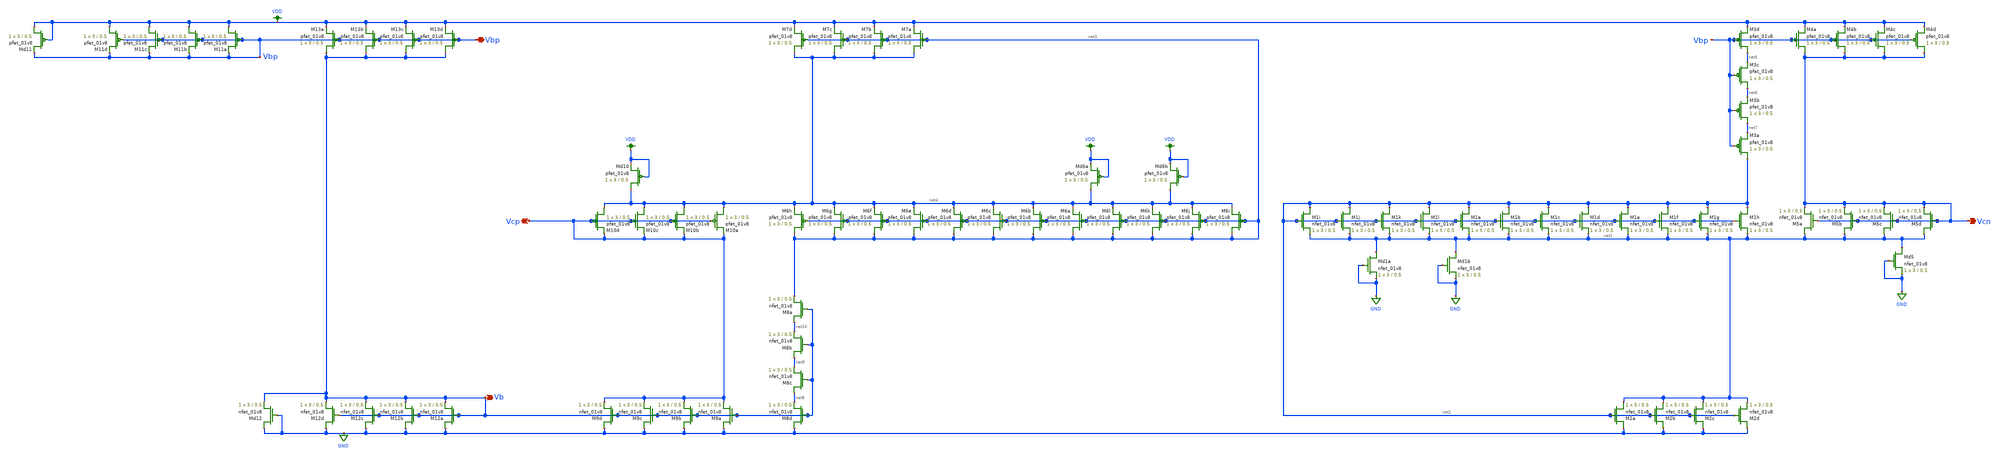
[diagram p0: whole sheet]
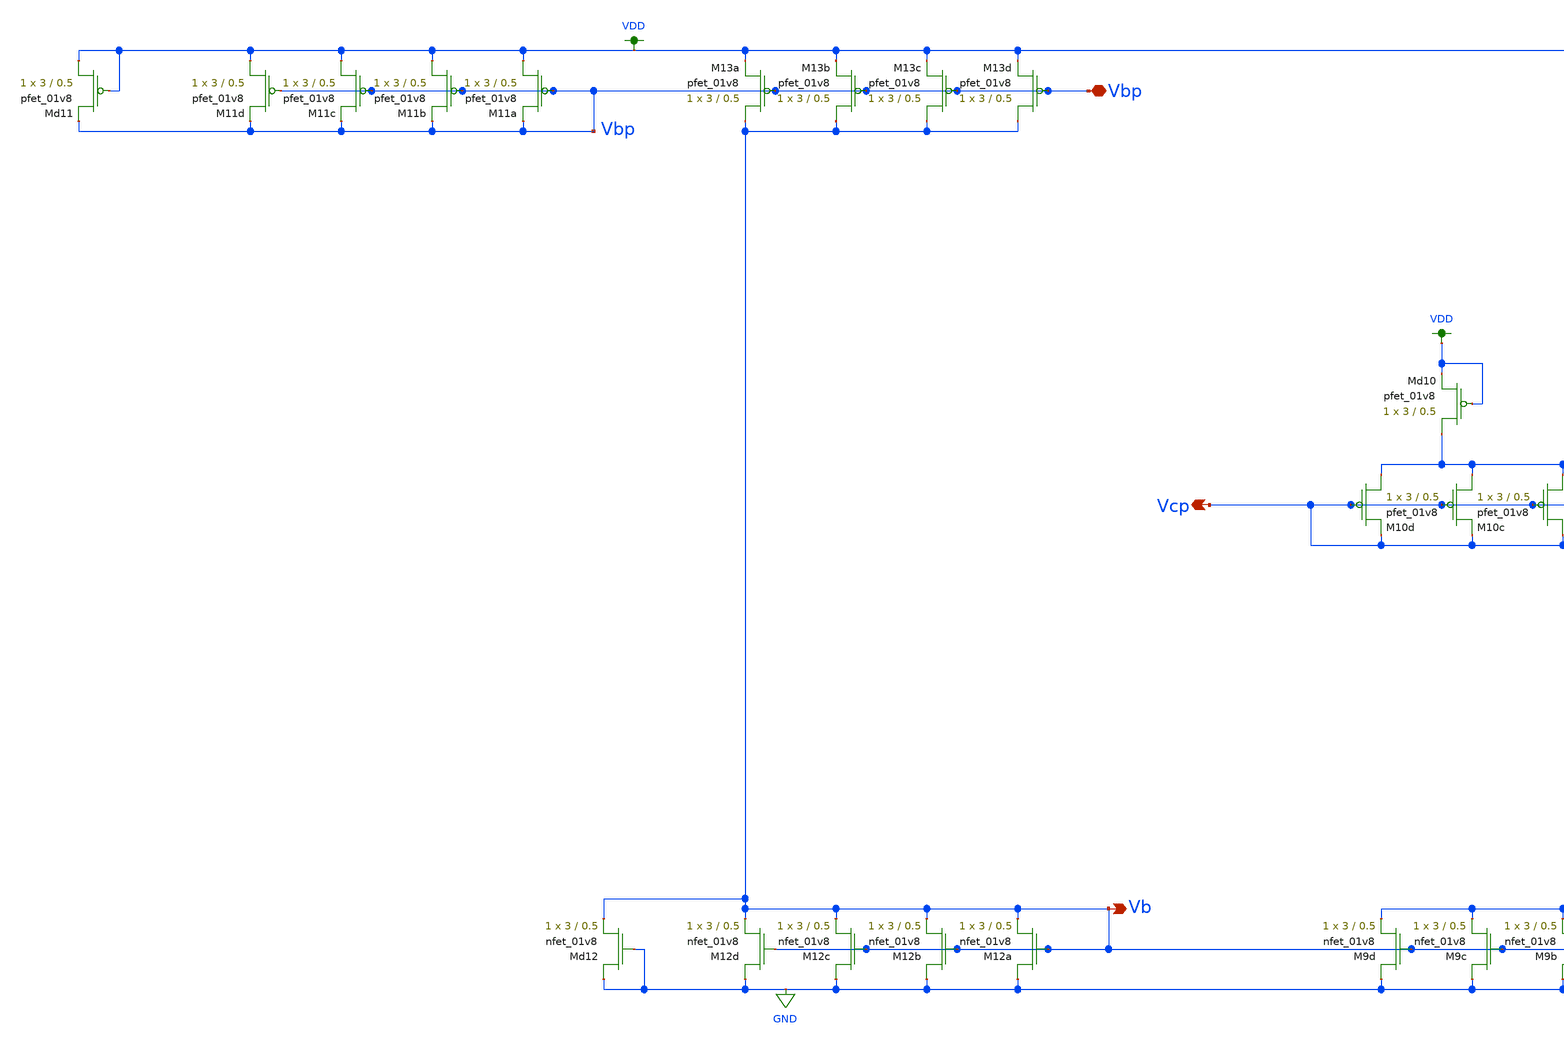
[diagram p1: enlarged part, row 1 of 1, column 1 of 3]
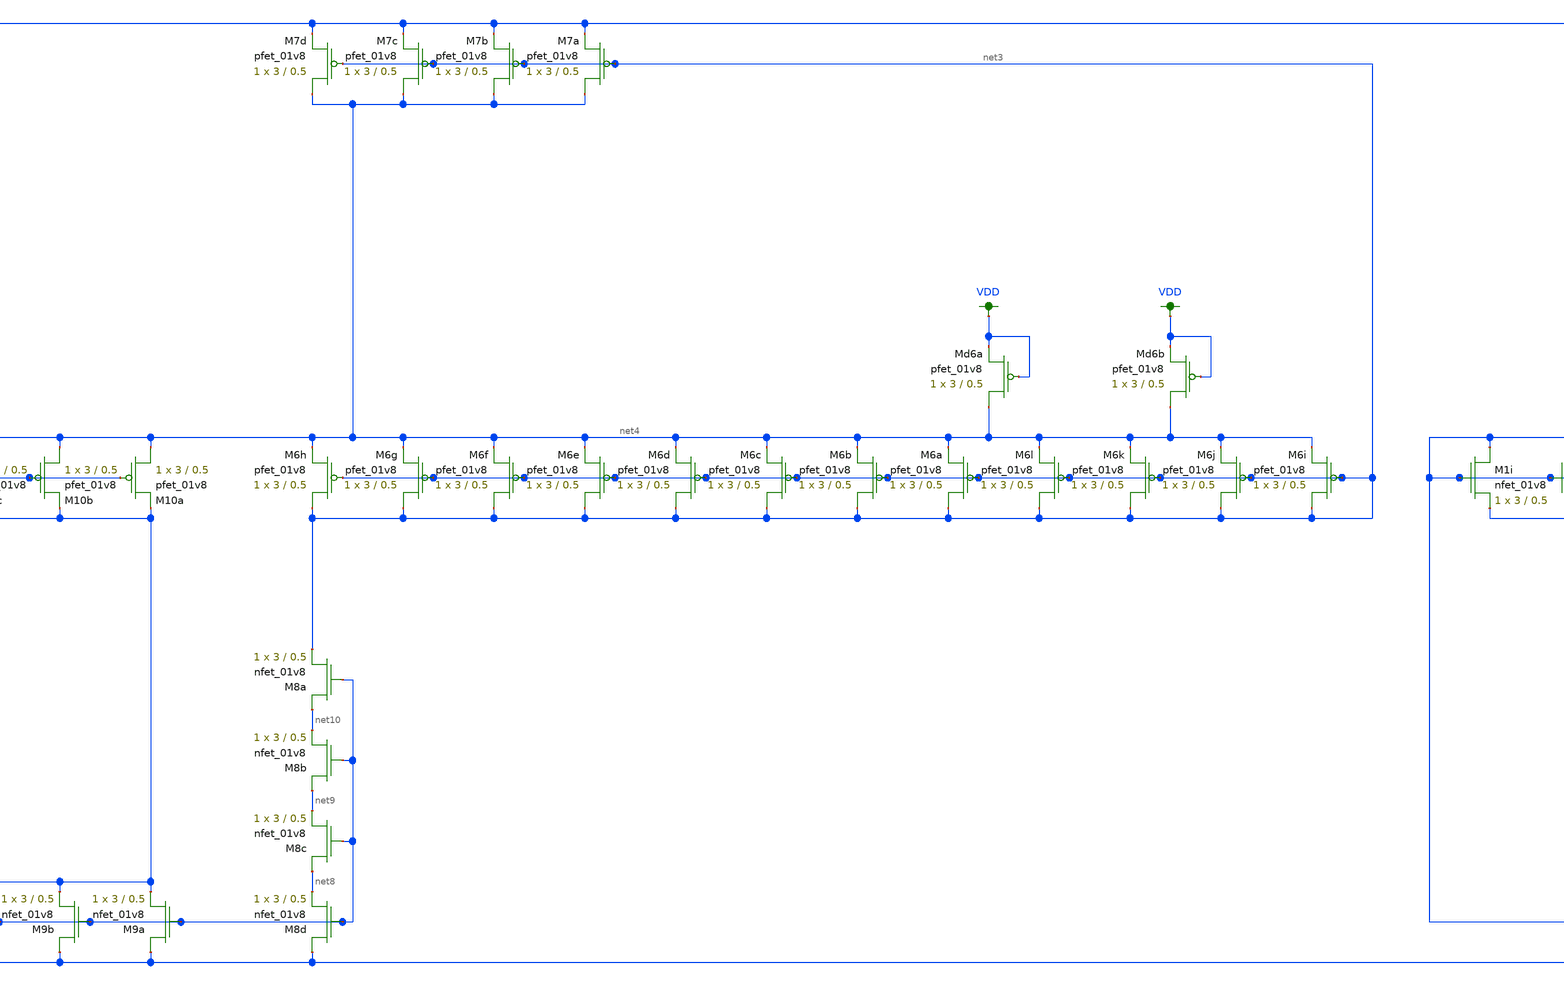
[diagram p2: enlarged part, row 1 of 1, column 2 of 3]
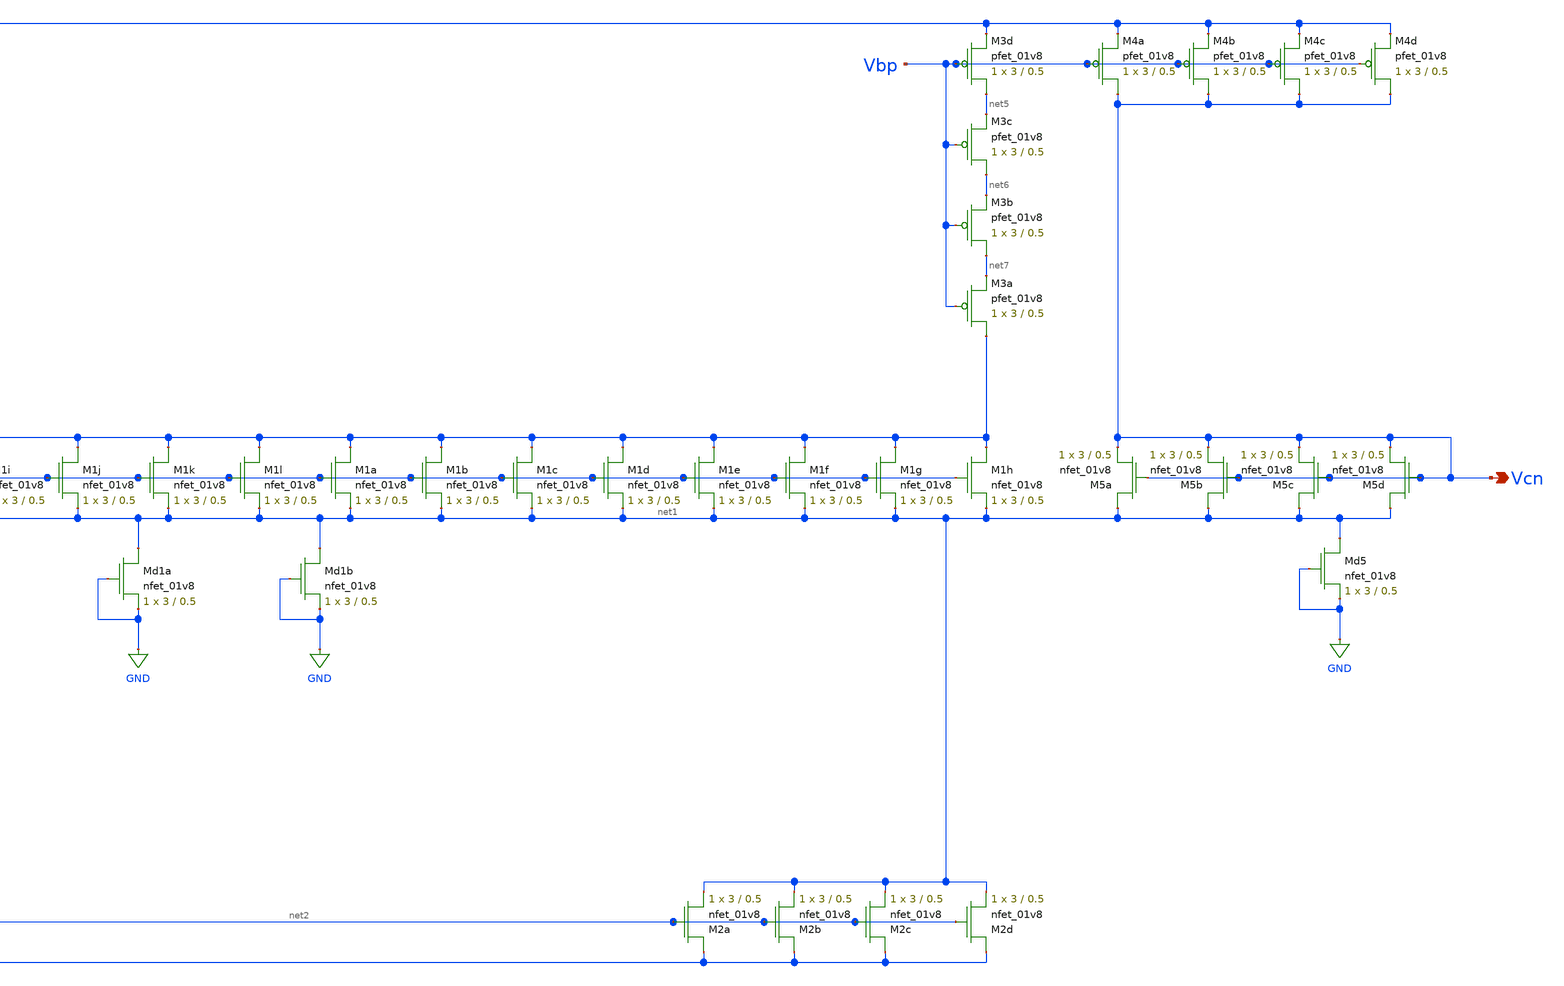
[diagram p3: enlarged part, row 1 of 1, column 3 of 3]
** sch_path: xschem/other_project_files/bias_schematic_lvs.sch
**.subckt bias_schematic_lvs Vcp Vbp Vcn Vb
*.opin Vcp
*.iopin Vbp
*.opin Vcn
*.opin Vb
XM1a net2 net2 net1 GND sky130_fd_pr__nfet_01v8 L=0.5 W=3 nf=1 ad='int((nf+1)/2) * W/nf * 0.29' as='int((nf+2)/2) * W/nf * 0.29'
+ pd='2*int((nf+1)/2) * (W/nf + 0.29)' ps='2*int((nf+2)/2) * (W/nf + 0.29)' nrd='0.29 / W' nrs='0.29 / W'
+ sa=0 sb=0 sd=0 mult=1 m=1
XM1b net2 net2 net1 GND sky130_fd_pr__nfet_01v8 L=0.5 W=3 nf=1 ad='int((nf+1)/2) * W/nf * 0.29' as='int((nf+2)/2) * W/nf * 0.29'
+ pd='2*int((nf+1)/2) * (W/nf + 0.29)' ps='2*int((nf+2)/2) * (W/nf + 0.29)' nrd='0.29 / W' nrs='0.29 / W'
+ sa=0 sb=0 sd=0 mult=1 m=1
XM1c net2 net2 net1 GND sky130_fd_pr__nfet_01v8 L=0.5 W=3 nf=1 ad='int((nf+1)/2) * W/nf * 0.29' as='int((nf+2)/2) * W/nf * 0.29'
+ pd='2*int((nf+1)/2) * (W/nf + 0.29)' ps='2*int((nf+2)/2) * (W/nf + 0.29)' nrd='0.29 / W' nrs='0.29 / W'
+ sa=0 sb=0 sd=0 mult=1 m=1
XM1d net2 net2 net1 GND sky130_fd_pr__nfet_01v8 L=0.5 W=3 nf=1 ad='int((nf+1)/2) * W/nf * 0.29' as='int((nf+2)/2) * W/nf * 0.29'
+ pd='2*int((nf+1)/2) * (W/nf + 0.29)' ps='2*int((nf+2)/2) * (W/nf + 0.29)' nrd='0.29 / W' nrs='0.29 / W'
+ sa=0 sb=0 sd=0 mult=1 m=1
XM2a GND net2 net1 GND sky130_fd_pr__nfet_01v8 L=0.5 W=3 nf=1 ad='int((nf+1)/2) * W/nf * 0.29' as='int((nf+2)/2) * W/nf * 0.29'
+ pd='2*int((nf+1)/2) * (W/nf + 0.29)' ps='2*int((nf+2)/2) * (W/nf + 0.29)' nrd='0.29 / W' nrs='0.29 / W'
+ sa=0 sb=0 sd=0 mult=1 m=1
XM2b GND net2 net1 GND sky130_fd_pr__nfet_01v8 L=0.5 W=3 nf=1 ad='int((nf+1)/2) * W/nf * 0.29' as='int((nf+2)/2) * W/nf * 0.29'
+ pd='2*int((nf+1)/2) * (W/nf + 0.29)' ps='2*int((nf+2)/2) * (W/nf + 0.29)' nrd='0.29 / W' nrs='0.29 / W'
+ sa=0 sb=0 sd=0 mult=1 m=1
XM2c GND net2 net1 GND sky130_fd_pr__nfet_01v8 L=0.5 W=3 nf=1 ad='int((nf+1)/2) * W/nf * 0.29' as='int((nf+2)/2) * W/nf * 0.29'
+ pd='2*int((nf+1)/2) * (W/nf + 0.29)' ps='2*int((nf+2)/2) * (W/nf + 0.29)' nrd='0.29 / W' nrs='0.29 / W'
+ sa=0 sb=0 sd=0 mult=1 m=1
XM2d GND net2 net1 GND sky130_fd_pr__nfet_01v8 L=0.5 W=3 nf=1 ad='int((nf+1)/2) * W/nf * 0.29' as='int((nf+2)/2) * W/nf * 0.29'
+ pd='2*int((nf+1)/2) * (W/nf + 0.29)' ps='2*int((nf+2)/2) * (W/nf + 0.29)' nrd='0.29 / W' nrs='0.29 / W'
+ sa=0 sb=0 sd=0 mult=1 m=1
XM3a net2 Vbp net7 VDD sky130_fd_pr__pfet_01v8 L=0.5 W=3 nf=1 ad='int((nf+1)/2) * W/nf * 0.29' as='int((nf+2)/2) * W/nf * 0.29'
+ pd='2*int((nf+1)/2) * (W/nf + 0.29)' ps='2*int((nf+2)/2) * (W/nf + 0.29)' nrd='0.29 / W' nrs='0.29 / W'
+ sa=0 sb=0 sd=0 mult=1 m=1
XM3b net7 Vbp net6 VDD sky130_fd_pr__pfet_01v8 L=0.5 W=3 nf=1 ad='int((nf+1)/2) * W/nf * 0.29' as='int((nf+2)/2) * W/nf * 0.29'
+ pd='2*int((nf+1)/2) * (W/nf + 0.29)' ps='2*int((nf+2)/2) * (W/nf + 0.29)' nrd='0.29 / W' nrs='0.29 / W'
+ sa=0 sb=0 sd=0 mult=1 m=1
XM3c net6 Vbp net5 VDD sky130_fd_pr__pfet_01v8 L=0.5 W=3 nf=1 ad='int((nf+1)/2) * W/nf * 0.29' as='int((nf+2)/2) * W/nf * 0.29'
+ pd='2*int((nf+1)/2) * (W/nf + 0.29)' ps='2*int((nf+2)/2) * (W/nf + 0.29)' nrd='0.29 / W' nrs='0.29 / W'
+ sa=0 sb=0 sd=0 mult=1 m=1
XM3d net5 Vbp VDD VDD sky130_fd_pr__pfet_01v8 L=0.5 W=3 nf=1 ad='int((nf+1)/2) * W/nf * 0.29' as='int((nf+2)/2) * W/nf * 0.29'
+ pd='2*int((nf+1)/2) * (W/nf + 0.29)' ps='2*int((nf+2)/2) * (W/nf + 0.29)' nrd='0.29 / W' nrs='0.29 / W'
+ sa=0 sb=0 sd=0 mult=1 m=1
XM4a Vcn Vbp VDD VDD sky130_fd_pr__pfet_01v8 L=0.5 W=3 nf=1 ad='int((nf+1)/2) * W/nf * 0.29' as='int((nf+2)/2) * W/nf * 0.29'
+ pd='2*int((nf+1)/2) * (W/nf + 0.29)' ps='2*int((nf+2)/2) * (W/nf + 0.29)' nrd='0.29 / W' nrs='0.29 / W'
+ sa=0 sb=0 sd=0 mult=1 m=1
XM4b Vcn Vbp VDD VDD sky130_fd_pr__pfet_01v8 L=0.5 W=3 nf=1 ad='int((nf+1)/2) * W/nf * 0.29' as='int((nf+2)/2) * W/nf * 0.29'
+ pd='2*int((nf+1)/2) * (W/nf + 0.29)' ps='2*int((nf+2)/2) * (W/nf + 0.29)' nrd='0.29 / W' nrs='0.29 / W'
+ sa=0 sb=0 sd=0 mult=1 m=1
XM4c Vcn Vbp VDD VDD sky130_fd_pr__pfet_01v8 L=0.5 W=3 nf=1 ad='int((nf+1)/2) * W/nf * 0.29' as='int((nf+2)/2) * W/nf * 0.29'
+ pd='2*int((nf+1)/2) * (W/nf + 0.29)' ps='2*int((nf+2)/2) * (W/nf + 0.29)' nrd='0.29 / W' nrs='0.29 / W'
+ sa=0 sb=0 sd=0 mult=1 m=1
XM4d Vcn Vbp VDD VDD sky130_fd_pr__pfet_01v8 L=0.5 W=3 nf=1 ad='int((nf+1)/2) * W/nf * 0.29' as='int((nf+2)/2) * W/nf * 0.29'
+ pd='2*int((nf+1)/2) * (W/nf + 0.29)' ps='2*int((nf+2)/2) * (W/nf + 0.29)' nrd='0.29 / W' nrs='0.29 / W'
+ sa=0 sb=0 sd=0 mult=1 m=1
XM11a VDD Vbp Vbp VDD sky130_fd_pr__pfet_01v8 L=0.5 W=3 nf=1 ad='int((nf+1)/2) * W/nf * 0.29' as='int((nf+2)/2) * W/nf * 0.29'
+ pd='2*int((nf+1)/2) * (W/nf + 0.29)' ps='2*int((nf+2)/2) * (W/nf + 0.29)' nrd='0.29 / W' nrs='0.29 / W'
+ sa=0 sb=0 sd=0 mult=1 m=1
XM11b VDD Vbp Vbp VDD sky130_fd_pr__pfet_01v8 L=0.5 W=3 nf=1 ad='int((nf+1)/2) * W/nf * 0.29' as='int((nf+2)/2) * W/nf * 0.29'
+ pd='2*int((nf+1)/2) * (W/nf + 0.29)' ps='2*int((nf+2)/2) * (W/nf + 0.29)' nrd='0.29 / W' nrs='0.29 / W'
+ sa=0 sb=0 sd=0 mult=1 m=1
XM11c VDD Vbp Vbp VDD sky130_fd_pr__pfet_01v8 L=0.5 W=3 nf=1 ad='int((nf+1)/2) * W/nf * 0.29' as='int((nf+2)/2) * W/nf * 0.29'
+ pd='2*int((nf+1)/2) * (W/nf + 0.29)' ps='2*int((nf+2)/2) * (W/nf + 0.29)' nrd='0.29 / W' nrs='0.29 / W'
+ sa=0 sb=0 sd=0 mult=1 m=1
XM11d VDD Vbp Vbp VDD sky130_fd_pr__pfet_01v8 L=0.5 W=3 nf=1 ad='int((nf+1)/2) * W/nf * 0.29' as='int((nf+2)/2) * W/nf * 0.29'
+ pd='2*int((nf+1)/2) * (W/nf + 0.29)' ps='2*int((nf+2)/2) * (W/nf + 0.29)' nrd='0.29 / W' nrs='0.29 / W'
+ sa=0 sb=0 sd=0 mult=1 m=1
XM5a net1 Vcn Vcn GND sky130_fd_pr__nfet_01v8 L=0.5 W=3 nf=1 ad='int((nf+1)/2) * W/nf * 0.29' as='int((nf+2)/2) * W/nf * 0.29'
+ pd='2*int((nf+1)/2) * (W/nf + 0.29)' ps='2*int((nf+2)/2) * (W/nf + 0.29)' nrd='0.29 / W' nrs='0.29 / W'
+ sa=0 sb=0 sd=0 mult=1 m=1
XM5b net1 Vcn Vcn GND sky130_fd_pr__nfet_01v8 L=0.5 W=3 nf=1 ad='int((nf+1)/2) * W/nf * 0.29' as='int((nf+2)/2) * W/nf * 0.29'
+ pd='2*int((nf+1)/2) * (W/nf + 0.29)' ps='2*int((nf+2)/2) * (W/nf + 0.29)' nrd='0.29 / W' nrs='0.29 / W'
+ sa=0 sb=0 sd=0 mult=1 m=1
XM5c net1 Vcn Vcn GND sky130_fd_pr__nfet_01v8 L=0.5 W=3 nf=1 ad='int((nf+1)/2) * W/nf * 0.29' as='int((nf+2)/2) * W/nf * 0.29'
+ pd='2*int((nf+1)/2) * (W/nf + 0.29)' ps='2*int((nf+2)/2) * (W/nf + 0.29)' nrd='0.29 / W' nrs='0.29 / W'
+ sa=0 sb=0 sd=0 mult=1 m=1
XM5d net1 Vcn Vcn GND sky130_fd_pr__nfet_01v8 L=0.5 W=3 nf=1 ad='int((nf+1)/2) * W/nf * 0.29' as='int((nf+2)/2) * W/nf * 0.29'
+ pd='2*int((nf+1)/2) * (W/nf + 0.29)' ps='2*int((nf+2)/2) * (W/nf + 0.29)' nrd='0.29 / W' nrs='0.29 / W'
+ sa=0 sb=0 sd=0 mult=1 m=1
XM8a net10 Vb net3 GND sky130_fd_pr__nfet_01v8 L=0.5 W=3 nf=1 ad='int((nf+1)/2) * W/nf * 0.29' as='int((nf+2)/2) * W/nf * 0.29'
+ pd='2*int((nf+1)/2) * (W/nf + 0.29)' ps='2*int((nf+2)/2) * (W/nf + 0.29)' nrd='0.29 / W' nrs='0.29 / W'
+ sa=0 sb=0 sd=0 mult=1 m=1
XM8b net9 Vb net10 GND sky130_fd_pr__nfet_01v8 L=0.5 W=3 nf=1 ad='int((nf+1)/2) * W/nf * 0.29' as='int((nf+2)/2) * W/nf * 0.29'
+ pd='2*int((nf+1)/2) * (W/nf + 0.29)' ps='2*int((nf+2)/2) * (W/nf + 0.29)' nrd='0.29 / W' nrs='0.29 / W'
+ sa=0 sb=0 sd=0 mult=1 m=1
XM8c net8 Vb net9 GND sky130_fd_pr__nfet_01v8 L=0.5 W=3 nf=1 ad='int((nf+1)/2) * W/nf * 0.29' as='int((nf+2)/2) * W/nf * 0.29'
+ pd='2*int((nf+1)/2) * (W/nf + 0.29)' ps='2*int((nf+2)/2) * (W/nf + 0.29)' nrd='0.29 / W' nrs='0.29 / W'
+ sa=0 sb=0 sd=0 mult=1 m=1
XM8d GND Vb net8 GND sky130_fd_pr__nfet_01v8 L=0.5 W=3 nf=1 ad='int((nf+1)/2) * W/nf * 0.29' as='int((nf+2)/2) * W/nf * 0.29'
+ pd='2*int((nf+1)/2) * (W/nf + 0.29)' ps='2*int((nf+2)/2) * (W/nf + 0.29)' nrd='0.29 / W' nrs='0.29 / W'
+ sa=0 sb=0 sd=0 mult=1 m=1
XM6a net3 net3 net4 VDD sky130_fd_pr__pfet_01v8 L=0.5 W=3 nf=1 ad='int((nf+1)/2) * W/nf * 0.29' as='int((nf+2)/2) * W/nf * 0.29'
+ pd='2*int((nf+1)/2) * (W/nf + 0.29)' ps='2*int((nf+2)/2) * (W/nf + 0.29)' nrd='0.29 / W' nrs='0.29 / W'
+ sa=0 sb=0 sd=0 mult=1 m=1
XM6b net3 net3 net4 VDD sky130_fd_pr__pfet_01v8 L=0.5 W=3 nf=1 ad='int((nf+1)/2) * W/nf * 0.29' as='int((nf+2)/2) * W/nf * 0.29'
+ pd='2*int((nf+1)/2) * (W/nf + 0.29)' ps='2*int((nf+2)/2) * (W/nf + 0.29)' nrd='0.29 / W' nrs='0.29 / W'
+ sa=0 sb=0 sd=0 mult=1 m=1
XM6c net3 net3 net4 VDD sky130_fd_pr__pfet_01v8 L=0.5 W=3 nf=1 ad='int((nf+1)/2) * W/nf * 0.29' as='int((nf+2)/2) * W/nf * 0.29'
+ pd='2*int((nf+1)/2) * (W/nf + 0.29)' ps='2*int((nf+2)/2) * (W/nf + 0.29)' nrd='0.29 / W' nrs='0.29 / W'
+ sa=0 sb=0 sd=0 mult=1 m=1
XM6d net3 net3 net4 VDD sky130_fd_pr__pfet_01v8 L=0.5 W=3 nf=1 ad='int((nf+1)/2) * W/nf * 0.29' as='int((nf+2)/2) * W/nf * 0.29'
+ pd='2*int((nf+1)/2) * (W/nf + 0.29)' ps='2*int((nf+2)/2) * (W/nf + 0.29)' nrd='0.29 / W' nrs='0.29 / W'
+ sa=0 sb=0 sd=0 mult=1 m=1
XM7a net4 net3 VDD VDD sky130_fd_pr__pfet_01v8 L=0.5 W=3 nf=1 ad='int((nf+1)/2) * W/nf * 0.29' as='int((nf+2)/2) * W/nf * 0.29'
+ pd='2*int((nf+1)/2) * (W/nf + 0.29)' ps='2*int((nf+2)/2) * (W/nf + 0.29)' nrd='0.29 / W' nrs='0.29 / W'
+ sa=0 sb=0 sd=0 mult=1 m=1
XM7b net4 net3 VDD VDD sky130_fd_pr__pfet_01v8 L=0.5 W=3 nf=1 ad='int((nf+1)/2) * W/nf * 0.29' as='int((nf+2)/2) * W/nf * 0.29'
+ pd='2*int((nf+1)/2) * (W/nf + 0.29)' ps='2*int((nf+2)/2) * (W/nf + 0.29)' nrd='0.29 / W' nrs='0.29 / W'
+ sa=0 sb=0 sd=0 mult=1 m=1
XM7c net4 net3 VDD VDD sky130_fd_pr__pfet_01v8 L=0.5 W=3 nf=1 ad='int((nf+1)/2) * W/nf * 0.29' as='int((nf+2)/2) * W/nf * 0.29'
+ pd='2*int((nf+1)/2) * (W/nf + 0.29)' ps='2*int((nf+2)/2) * (W/nf + 0.29)' nrd='0.29 / W' nrs='0.29 / W'
+ sa=0 sb=0 sd=0 mult=1 m=1
XM7d net4 net3 VDD VDD sky130_fd_pr__pfet_01v8 L=0.5 W=3 nf=1 ad='int((nf+1)/2) * W/nf * 0.29' as='int((nf+2)/2) * W/nf * 0.29'
+ pd='2*int((nf+1)/2) * (W/nf + 0.29)' ps='2*int((nf+2)/2) * (W/nf + 0.29)' nrd='0.29 / W' nrs='0.29 / W'
+ sa=0 sb=0 sd=0 mult=1 m=1
XM10d net4 Vcp Vcp VDD sky130_fd_pr__pfet_01v8 L=0.5 W=3 nf=1 ad='int((nf+1)/2) * W/nf * 0.29' as='int((nf+2)/2) * W/nf * 0.29'
+ pd='2*int((nf+1)/2) * (W/nf + 0.29)' ps='2*int((nf+2)/2) * (W/nf + 0.29)' nrd='0.29 / W' nrs='0.29 / W'
+ sa=0 sb=0 sd=0 mult=1 m=1
XM10c net4 Vcp Vcp VDD sky130_fd_pr__pfet_01v8 L=0.5 W=3 nf=1 ad='int((nf+1)/2) * W/nf * 0.29' as='int((nf+2)/2) * W/nf * 0.29'
+ pd='2*int((nf+1)/2) * (W/nf + 0.29)' ps='2*int((nf+2)/2) * (W/nf + 0.29)' nrd='0.29 / W' nrs='0.29 / W'
+ sa=0 sb=0 sd=0 mult=1 m=1
XM10b net4 Vcp Vcp VDD sky130_fd_pr__pfet_01v8 L=0.5 W=3 nf=1 ad='int((nf+1)/2) * W/nf * 0.29' as='int((nf+2)/2) * W/nf * 0.29'
+ pd='2*int((nf+1)/2) * (W/nf + 0.29)' ps='2*int((nf+2)/2) * (W/nf + 0.29)' nrd='0.29 / W' nrs='0.29 / W'
+ sa=0 sb=0 sd=0 mult=1 m=1
XM10a net4 Vcp Vcp VDD sky130_fd_pr__pfet_01v8 L=0.5 W=3 nf=1 ad='int((nf+1)/2) * W/nf * 0.29' as='int((nf+2)/2) * W/nf * 0.29'
+ pd='2*int((nf+1)/2) * (W/nf + 0.29)' ps='2*int((nf+2)/2) * (W/nf + 0.29)' nrd='0.29 / W' nrs='0.29 / W'
+ sa=0 sb=0 sd=0 mult=1 m=1
XM9a GND Vb Vcp GND sky130_fd_pr__nfet_01v8 L=0.5 W=3 nf=1 ad='int((nf+1)/2) * W/nf * 0.29' as='int((nf+2)/2) * W/nf * 0.29'
+ pd='2*int((nf+1)/2) * (W/nf + 0.29)' ps='2*int((nf+2)/2) * (W/nf + 0.29)' nrd='0.29 / W' nrs='0.29 / W'
+ sa=0 sb=0 sd=0 mult=1 m=1
XM9b GND Vb Vcp GND sky130_fd_pr__nfet_01v8 L=0.5 W=3 nf=1 ad='int((nf+1)/2) * W/nf * 0.29' as='int((nf+2)/2) * W/nf * 0.29'
+ pd='2*int((nf+1)/2) * (W/nf + 0.29)' ps='2*int((nf+2)/2) * (W/nf + 0.29)' nrd='0.29 / W' nrs='0.29 / W'
+ sa=0 sb=0 sd=0 mult=1 m=1
XM9c GND Vb Vcp GND sky130_fd_pr__nfet_01v8 L=0.5 W=3 nf=1 ad='int((nf+1)/2) * W/nf * 0.29' as='int((nf+2)/2) * W/nf * 0.29'
+ pd='2*int((nf+1)/2) * (W/nf + 0.29)' ps='2*int((nf+2)/2) * (W/nf + 0.29)' nrd='0.29 / W' nrs='0.29 / W'
+ sa=0 sb=0 sd=0 mult=1 m=1
XM9d GND Vb Vcp GND sky130_fd_pr__nfet_01v8 L=0.5 W=3 nf=1 ad='int((nf+1)/2) * W/nf * 0.29' as='int((nf+2)/2) * W/nf * 0.29'
+ pd='2*int((nf+1)/2) * (W/nf + 0.29)' ps='2*int((nf+2)/2) * (W/nf + 0.29)' nrd='0.29 / W' nrs='0.29 / W'
+ sa=0 sb=0 sd=0 mult=1 m=1
XM12a GND Vb Vb GND sky130_fd_pr__nfet_01v8 L=0.5 W=3 nf=1 ad='int((nf+1)/2) * W/nf * 0.29' as='int((nf+2)/2) * W/nf * 0.29'
+ pd='2*int((nf+1)/2) * (W/nf + 0.29)' ps='2*int((nf+2)/2) * (W/nf + 0.29)' nrd='0.29 / W' nrs='0.29 / W'
+ sa=0 sb=0 sd=0 mult=1 m=1
XM12b GND Vb Vb GND sky130_fd_pr__nfet_01v8 L=0.5 W=3 nf=1 ad='int((nf+1)/2) * W/nf * 0.29' as='int((nf+2)/2) * W/nf * 0.29'
+ pd='2*int((nf+1)/2) * (W/nf + 0.29)' ps='2*int((nf+2)/2) * (W/nf + 0.29)' nrd='0.29 / W' nrs='0.29 / W'
+ sa=0 sb=0 sd=0 mult=1 m=1
XM12c GND Vb Vb GND sky130_fd_pr__nfet_01v8 L=0.5 W=3 nf=1 ad='int((nf+1)/2) * W/nf * 0.29' as='int((nf+2)/2) * W/nf * 0.29'
+ pd='2*int((nf+1)/2) * (W/nf + 0.29)' ps='2*int((nf+2)/2) * (W/nf + 0.29)' nrd='0.29 / W' nrs='0.29 / W'
+ sa=0 sb=0 sd=0 mult=1 m=1
XM12d GND Vb Vb GND sky130_fd_pr__nfet_01v8 L=0.5 W=3 nf=1 ad='int((nf+1)/2) * W/nf * 0.29' as='int((nf+2)/2) * W/nf * 0.29'
+ pd='2*int((nf+1)/2) * (W/nf + 0.29)' ps='2*int((nf+2)/2) * (W/nf + 0.29)' nrd='0.29 / W' nrs='0.29 / W'
+ sa=0 sb=0 sd=0 mult=1 m=1
XM13d Vb Vbp VDD VDD sky130_fd_pr__pfet_01v8 L=0.5 W=3 nf=1 ad='int((nf+1)/2) * W/nf * 0.29' as='int((nf+2)/2) * W/nf * 0.29'
+ pd='2*int((nf+1)/2) * (W/nf + 0.29)' ps='2*int((nf+2)/2) * (W/nf + 0.29)' nrd='0.29 / W' nrs='0.29 / W'
+ sa=0 sb=0 sd=0 mult=1 m=1
XM13c Vb Vbp VDD VDD sky130_fd_pr__pfet_01v8 L=0.5 W=3 nf=1 ad='int((nf+1)/2) * W/nf * 0.29' as='int((nf+2)/2) * W/nf * 0.29'
+ pd='2*int((nf+1)/2) * (W/nf + 0.29)' ps='2*int((nf+2)/2) * (W/nf + 0.29)' nrd='0.29 / W' nrs='0.29 / W'
+ sa=0 sb=0 sd=0 mult=1 m=1
XM13b Vb Vbp VDD VDD sky130_fd_pr__pfet_01v8 L=0.5 W=3 nf=1 ad='int((nf+1)/2) * W/nf * 0.29' as='int((nf+2)/2) * W/nf * 0.29'
+ pd='2*int((nf+1)/2) * (W/nf + 0.29)' ps='2*int((nf+2)/2) * (W/nf + 0.29)' nrd='0.29 / W' nrs='0.29 / W'
+ sa=0 sb=0 sd=0 mult=1 m=1
XM13a Vb Vbp VDD VDD sky130_fd_pr__pfet_01v8 L=0.5 W=3 nf=1 ad='int((nf+1)/2) * W/nf * 0.29' as='int((nf+2)/2) * W/nf * 0.29'
+ pd='2*int((nf+1)/2) * (W/nf + 0.29)' ps='2*int((nf+2)/2) * (W/nf + 0.29)' nrd='0.29 / W' nrs='0.29 / W'
+ sa=0 sb=0 sd=0 mult=1 m=1
XM1e net2 net2 net1 GND sky130_fd_pr__nfet_01v8 L=0.5 W=3 nf=1 ad='int((nf+1)/2) * W/nf * 0.29' as='int((nf+2)/2) * W/nf * 0.29'
+ pd='2*int((nf+1)/2) * (W/nf + 0.29)' ps='2*int((nf+2)/2) * (W/nf + 0.29)' nrd='0.29 / W' nrs='0.29 / W'
+ sa=0 sb=0 sd=0 mult=1 m=1
XM1f net2 net2 net1 GND sky130_fd_pr__nfet_01v8 L=0.5 W=3 nf=1 ad='int((nf+1)/2) * W/nf * 0.29' as='int((nf+2)/2) * W/nf * 0.29'
+ pd='2*int((nf+1)/2) * (W/nf + 0.29)' ps='2*int((nf+2)/2) * (W/nf + 0.29)' nrd='0.29 / W' nrs='0.29 / W'
+ sa=0 sb=0 sd=0 mult=1 m=1
XM1g net2 net2 net1 GND sky130_fd_pr__nfet_01v8 L=0.5 W=3 nf=1 ad='int((nf+1)/2) * W/nf * 0.29' as='int((nf+2)/2) * W/nf * 0.29'
+ pd='2*int((nf+1)/2) * (W/nf + 0.29)' ps='2*int((nf+2)/2) * (W/nf + 0.29)' nrd='0.29 / W' nrs='0.29 / W'
+ sa=0 sb=0 sd=0 mult=1 m=1
XM1h net2 net2 net1 GND sky130_fd_pr__nfet_01v8 L=0.5 W=3 nf=1 ad='int((nf+1)/2) * W/nf * 0.29' as='int((nf+2)/2) * W/nf * 0.29'
+ pd='2*int((nf+1)/2) * (W/nf + 0.29)' ps='2*int((nf+2)/2) * (W/nf + 0.29)' nrd='0.29 / W' nrs='0.29 / W'
+ sa=0 sb=0 sd=0 mult=1 m=1
XM6e net3 net3 net4 VDD sky130_fd_pr__pfet_01v8 L=0.5 W=3 nf=1 ad='int((nf+1)/2) * W/nf * 0.29' as='int((nf+2)/2) * W/nf * 0.29'
+ pd='2*int((nf+1)/2) * (W/nf + 0.29)' ps='2*int((nf+2)/2) * (W/nf + 0.29)' nrd='0.29 / W' nrs='0.29 / W'
+ sa=0 sb=0 sd=0 mult=1 m=1
XM6f net3 net3 net4 VDD sky130_fd_pr__pfet_01v8 L=0.5 W=3 nf=1 ad='int((nf+1)/2) * W/nf * 0.29' as='int((nf+2)/2) * W/nf * 0.29'
+ pd='2*int((nf+1)/2) * (W/nf + 0.29)' ps='2*int((nf+2)/2) * (W/nf + 0.29)' nrd='0.29 / W' nrs='0.29 / W'
+ sa=0 sb=0 sd=0 mult=1 m=1
XM6g net3 net3 net4 VDD sky130_fd_pr__pfet_01v8 L=0.5 W=3 nf=1 ad='int((nf+1)/2) * W/nf * 0.29' as='int((nf+2)/2) * W/nf * 0.29'
+ pd='2*int((nf+1)/2) * (W/nf + 0.29)' ps='2*int((nf+2)/2) * (W/nf + 0.29)' nrd='0.29 / W' nrs='0.29 / W'
+ sa=0 sb=0 sd=0 mult=1 m=1
XM6h net3 net3 net4 VDD sky130_fd_pr__pfet_01v8 L=0.5 W=3 nf=1 ad='int((nf+1)/2) * W/nf * 0.29' as='int((nf+2)/2) * W/nf * 0.29'
+ pd='2*int((nf+1)/2) * (W/nf + 0.29)' ps='2*int((nf+2)/2) * (W/nf + 0.29)' nrd='0.29 / W' nrs='0.29 / W'
+ sa=0 sb=0 sd=0 mult=1 m=1
XM1i net2 net2 net1 GND sky130_fd_pr__nfet_01v8 L=0.5 W=3 nf=1 ad='int((nf+1)/2) * W/nf * 0.29' as='int((nf+2)/2) * W/nf * 0.29'
+ pd='2*int((nf+1)/2) * (W/nf + 0.29)' ps='2*int((nf+2)/2) * (W/nf + 0.29)' nrd='0.29 / W' nrs='0.29 / W'
+ sa=0 sb=0 sd=0 mult=1 m=1
XM1j net2 net2 net1 GND sky130_fd_pr__nfet_01v8 L=0.5 W=3 nf=1 ad='int((nf+1)/2) * W/nf * 0.29' as='int((nf+2)/2) * W/nf * 0.29'
+ pd='2*int((nf+1)/2) * (W/nf + 0.29)' ps='2*int((nf+2)/2) * (W/nf + 0.29)' nrd='0.29 / W' nrs='0.29 / W'
+ sa=0 sb=0 sd=0 mult=1 m=1
XM1k net2 net2 net1 GND sky130_fd_pr__nfet_01v8 L=0.5 W=3 nf=1 ad='int((nf+1)/2) * W/nf * 0.29' as='int((nf+2)/2) * W/nf * 0.29'
+ pd='2*int((nf+1)/2) * (W/nf + 0.29)' ps='2*int((nf+2)/2) * (W/nf + 0.29)' nrd='0.29 / W' nrs='0.29 / W'
+ sa=0 sb=0 sd=0 mult=1 m=1
XM1l net2 net2 net1 GND sky130_fd_pr__nfet_01v8 L=0.5 W=3 nf=1 ad='int((nf+1)/2) * W/nf * 0.29' as='int((nf+2)/2) * W/nf * 0.29'
+ pd='2*int((nf+1)/2) * (W/nf + 0.29)' ps='2*int((nf+2)/2) * (W/nf + 0.29)' nrd='0.29 / W' nrs='0.29 / W'
+ sa=0 sb=0 sd=0 mult=1 m=1
XM6i net3 net3 net4 VDD sky130_fd_pr__pfet_01v8 L=0.5 W=3 nf=1 ad='int((nf+1)/2) * W/nf * 0.29' as='int((nf+2)/2) * W/nf * 0.29'
+ pd='2*int((nf+1)/2) * (W/nf + 0.29)' ps='2*int((nf+2)/2) * (W/nf + 0.29)' nrd='0.29 / W' nrs='0.29 / W'
+ sa=0 sb=0 sd=0 mult=1 m=1
XM6j net3 net3 net4 VDD sky130_fd_pr__pfet_01v8 L=0.5 W=3 nf=1 ad='int((nf+1)/2) * W/nf * 0.29' as='int((nf+2)/2) * W/nf * 0.29'
+ pd='2*int((nf+1)/2) * (W/nf + 0.29)' ps='2*int((nf+2)/2) * (W/nf + 0.29)' nrd='0.29 / W' nrs='0.29 / W'
+ sa=0 sb=0 sd=0 mult=1 m=1
XM6k net3 net3 net4 VDD sky130_fd_pr__pfet_01v8 L=0.5 W=3 nf=1 ad='int((nf+1)/2) * W/nf * 0.29' as='int((nf+2)/2) * W/nf * 0.29'
+ pd='2*int((nf+1)/2) * (W/nf + 0.29)' ps='2*int((nf+2)/2) * (W/nf + 0.29)' nrd='0.29 / W' nrs='0.29 / W'
+ sa=0 sb=0 sd=0 mult=1 m=1
XM6l net3 net3 net4 VDD sky130_fd_pr__pfet_01v8 L=0.5 W=3 nf=1 ad='int((nf+1)/2) * W/nf * 0.29' as='int((nf+2)/2) * W/nf * 0.29'
+ pd='2*int((nf+1)/2) * (W/nf + 0.29)' ps='2*int((nf+2)/2) * (W/nf + 0.29)' nrd='0.29 / W' nrs='0.29 / W'
+ sa=0 sb=0 sd=0 mult=1 m=1
XMd11 VDD VDD Vbp VDD sky130_fd_pr__pfet_01v8 L=0.5 W=3 nf=1 ad='int((nf+1)/2) * W/nf * 0.29' as='int((nf+2)/2) * W/nf * 0.29'
+ pd='2*int((nf+1)/2) * (W/nf + 0.29)' ps='2*int((nf+2)/2) * (W/nf + 0.29)' nrd='0.29 / W' nrs='0.29 / W'
+ sa=0 sb=0 sd=0 mult=1 m=1
XMd12 GND GND Vb GND sky130_fd_pr__nfet_01v8 L=0.5 W=3 nf=1 ad='int((nf+1)/2) * W/nf * 0.29' as='int((nf+2)/2) * W/nf * 0.29'
+ pd='2*int((nf+1)/2) * (W/nf + 0.29)' ps='2*int((nf+2)/2) * (W/nf + 0.29)' nrd='0.29 / W' nrs='0.29 / W'
+ sa=0 sb=0 sd=0 mult=1 m=1
XMd6b net4 VDD VDD VDD sky130_fd_pr__pfet_01v8 L=0.5 W=3 nf=1 ad='int((nf+1)/2) * W/nf * 0.29' as='int((nf+2)/2) * W/nf * 0.29'
+ pd='2*int((nf+1)/2) * (W/nf + 0.29)' ps='2*int((nf+2)/2) * (W/nf + 0.29)' nrd='0.29 / W' nrs='0.29 / W'
+ sa=0 sb=0 sd=0 mult=1 m=1
XMd6a net4 VDD VDD VDD sky130_fd_pr__pfet_01v8 L=0.5 W=3 nf=1 ad='int((nf+1)/2) * W/nf * 0.29' as='int((nf+2)/2) * W/nf * 0.29'
+ pd='2*int((nf+1)/2) * (W/nf + 0.29)' ps='2*int((nf+2)/2) * (W/nf + 0.29)' nrd='0.29 / W' nrs='0.29 / W'
+ sa=0 sb=0 sd=0 mult=1 m=1
XMd1a net1 GND GND GND sky130_fd_pr__nfet_01v8 L=0.5 W=3 nf=1 ad='int((nf+1)/2) * W/nf * 0.29' as='int((nf+2)/2) * W/nf * 0.29'
+ pd='2*int((nf+1)/2) * (W/nf + 0.29)' ps='2*int((nf+2)/2) * (W/nf + 0.29)' nrd='0.29 / W' nrs='0.29 / W'
+ sa=0 sb=0 sd=0 mult=1 m=1
XMd1b net1 GND GND GND sky130_fd_pr__nfet_01v8 L=0.5 W=3 nf=1 ad='int((nf+1)/2) * W/nf * 0.29' as='int((nf+2)/2) * W/nf * 0.29'
+ pd='2*int((nf+1)/2) * (W/nf + 0.29)' ps='2*int((nf+2)/2) * (W/nf + 0.29)' nrd='0.29 / W' nrs='0.29 / W'
+ sa=0 sb=0 sd=0 mult=1 m=1
XMd10 net4 VDD VDD VDD sky130_fd_pr__pfet_01v8 L=0.5 W=3 nf=1 ad='int((nf+1)/2) * W/nf * 0.29' as='int((nf+2)/2) * W/nf * 0.29'
+ pd='2*int((nf+1)/2) * (W/nf + 0.29)' ps='2*int((nf+2)/2) * (W/nf + 0.29)' nrd='0.29 / W' nrs='0.29 / W'
+ sa=0 sb=0 sd=0 mult=1 m=1
XMd5 net1 GND GND GND sky130_fd_pr__nfet_01v8 L=0.5 W=3 nf=1 ad='int((nf+1)/2) * W/nf * 0.29' as='int((nf+2)/2) * W/nf * 0.29'
+ pd='2*int((nf+1)/2) * (W/nf + 0.29)' ps='2*int((nf+2)/2) * (W/nf + 0.29)' nrd='0.29 / W' nrs='0.29 / W'
+ sa=0 sb=0 sd=0 mult=1 m=1
**.ends
.GLOBAL VDD
.GLOBAL GND
.end
